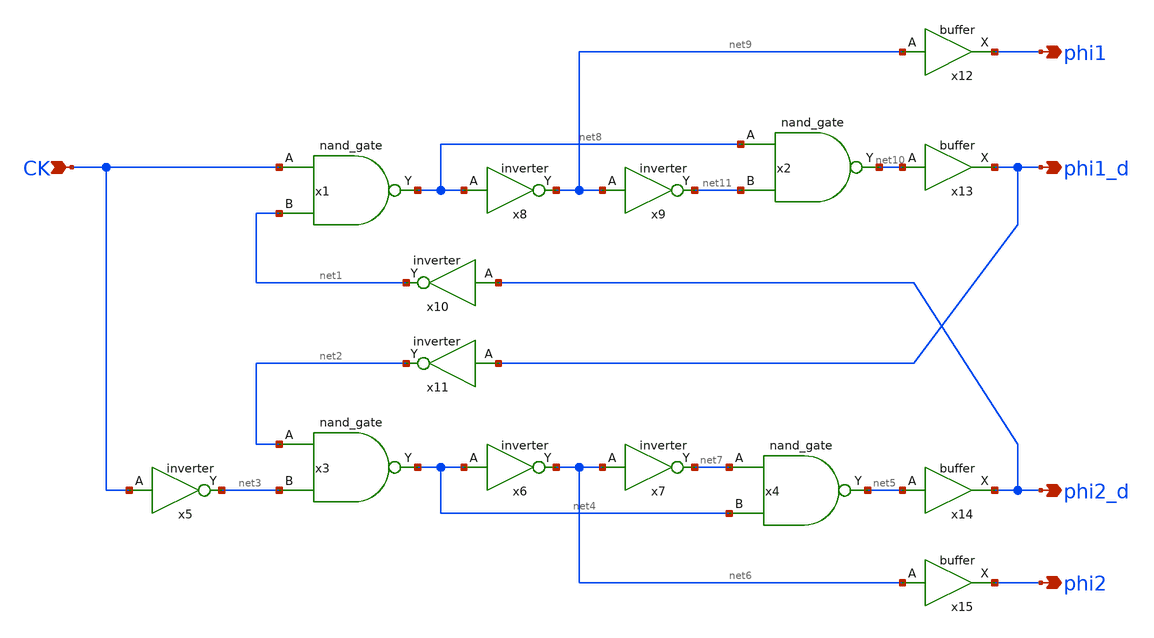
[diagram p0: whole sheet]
** sch_path: 3_real_circuits/clk_gen.sch
**.subckt clk_gen CK phi1 phi1_d phi2_d phi2
*.ipin CK
*.opin phi1
*.opin phi1_d
*.opin phi2_d
*.opin phi2
x1 CK net1 net8 nand_gate
x2 net8 net11 net10 nand_gate
x3 net2 net3 net4 nand_gate
x4 net7 net4 net5 nand_gate
x5 CK net3 inverter
x6 net4 net6 inverter
x7 net6 net7 inverter
x8 net8 net9 inverter
x9 net9 net11 inverter
x10 phi2_d net1 inverter
x11 phi1_d net2 inverter
x12 net9 phi1 buffer
x13 net10 phi1_d buffer
x14 net5 phi2_d buffer
x15 net6 phi2 buffer
**.ends

* expanding   symbol:  nand_gate.sym # of pins=3
** sym_path: 3_real_circuits/nand_gate.sym
** sch_path: 3_real_circuits/nand_gate.sch
.subckt nand_gate A B Y
*.ipin A
*.ipin B
*.opin Y
XM1 Y B VDD VDD sg13_hv_pmos w=0.3u l=0.4u ng=1 m=1 mm_ok=1
XM2 Y A VDD VDD sg13_hv_pmos w=0.3u l=0.4u ng=1 m=1 mm_ok=1
XM3 Y A net1 GND sg13_hv_nmos w=0.3u l=0.45u ng=1 m=1 mm_ok=1
XM4 net1 B GND GND sg13_hv_nmos w=0.3u l=0.45u ng=1 m=1 mm_ok=1
.ends


* expanding   symbol:  inverter.sym # of pins=2
** sym_path: 3_real_circuits/inverter.sym
** sch_path: 3_real_circuits/inverter.sch
.subckt inverter A Y
*.opin Y
*.ipin A
XM2 Y A GND GND sg13_hv_nmos w=0.3u l=0.45u ng=1 m=1 mm_ok=1
XM1 Y A VDD VDD sg13_hv_pmos w=0.3u l=0.4u ng=1 m=1 mm_ok=1
.ends


* expanding   symbol:  buffer.sym # of pins=2
** sym_path: 3_real_circuits/buffer.sym
** sch_path: 3_real_circuits/buffer.sch
.subckt buffer A X
*.ipin A
*.opin X
XM2 net1 A GND GND sg13_hv_nmos w=0.3u l=0.45u ng=1 m=1 mm_ok=1
XM1 net1 A VDD VDD sg13_hv_pmos w=0.3u l=0.4u ng=1 m=1 mm_ok=1
XM3 X net1 GND GND sg13_hv_nmos w=0.3u l=0.45u ng=1 m=1 mm_ok=1
XM4 X net1 VDD VDD sg13_hv_pmos w=0.3u l=0.4u ng=1 m=1 mm_ok=1
.ends

.GLOBAL GND
.GLOBAL VDD
.end
